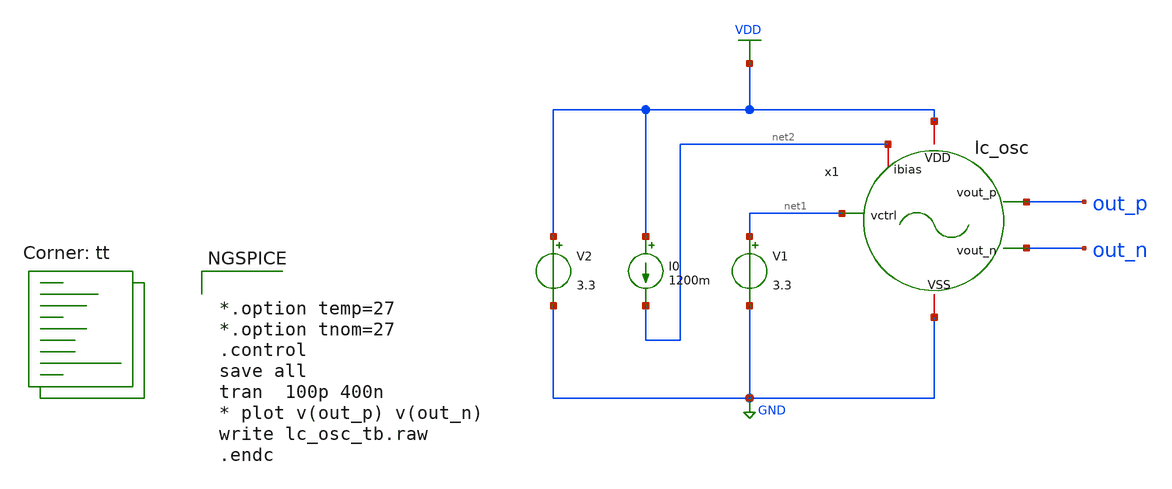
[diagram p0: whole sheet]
** sch_path: designs/libs/test_vco/lc_osc_tb.sch
* Copyright 2021 Stefan Frederik Schippers
* Licensed under the Apache License, Version 2.0 (the "License");
* you may not use this file except in compliance with the License.
* You may obtain a copy of the License at
* https://www.apache.org/licenses/LICENSE-2.0
* Unless required by applicable law or agreed to in writing, software
* distributed under the License is distributed on an "AS IS" BASIS,
* WITHOUT WARRANTIES OR CONDITIONS OF ANY KIND, either express or implied.
* See the License for the specific language governing permissions and
* limitations under the License.
**.subckt lc_osc_tb
V1 net1 GND 3.3
V2 VDD GND 3.3
I0 VDD net2 1200m
x1 VDD out_n out_p net1 GND net2 lc_osc
**** begin user architecture code


*.option temp=27
*.option tnom=27
.control
save all
tran  100p 400n
* plot v(out_p) v(out_n)
write lc_osc_tb.raw
.endc


.lib $::SKYWATER_MODELS/sky130.lib.spice tt
**** end user architecture code
**.ends

* expanding   symbol:  libs/test_vco/lc_osc.sym # of pins=6
** sym_path: designs/libs/test_vco/lc_osc.sym
** sch_path: designs/libs/test_vco/lc_osc.sch
.subckt lc_osc VDD vout_n vout_p vctrl VSS ibias
*.ipin vctrl
*.iopin VSS
*.iopin VDD
*.opin vout_p
*.opin vout_n
*.iopin ibias
L2 VDD vout_n 500p m=1
L3 VDD vout_p 500p m=1
XM4 ibias ibias VSS VSS sky130_fd_pr__nfet_g5v0d10v5 L=0.5 W=50 nf=1 ad='int((nf+1)/2) * W/nf * 0.29'
+ as='int((nf+2)/2) * W/nf * 0.29' pd='2*int((nf+1)/2) * (W/nf + 0.29)' ps='2*int((nf+2)/2) * (W/nf + 0.29)'
+ nrd='0.29 / W' nrs='0.29 / W' sa=0 sb=0 sd=0 mult=1 m=1
XM3 net1 ibias VSS VSS sky130_fd_pr__nfet_g5v0d10v5 L=0.5 W=50 nf=1 ad='int((nf+1)/2) * W/nf * 0.29'
+ as='int((nf+2)/2) * W/nf * 0.29' pd='2*int((nf+1)/2) * (W/nf + 0.29)' ps='2*int((nf+2)/2) * (W/nf + 0.29)'
+ nrd='0.29 / W' nrs='0.29 / W' sa=0 sb=0 sd=0 mult=1 m=1
XM1 vout_n vout_p net1 net1 sky130_fd_pr__nfet_g5v0d10v5 L=0.5 W=50 nf=1 ad='int((nf+1)/2) * W/nf * 0.29'
+ as='int((nf+2)/2) * W/nf * 0.29' pd='2*int((nf+1)/2) * (W/nf + 0.29)' ps='2*int((nf+2)/2) * (W/nf + 0.29)'
+ nrd='0.29 / W' nrs='0.29 / W' sa=0 sb=0 sd=0 mult=40 m=40
XM2 vout_p vout_n net1 net1 sky130_fd_pr__nfet_g5v0d10v5 L=0.5 W=50 nf=1 ad='int((nf+1)/2) * W/nf * 0.29'
+ as='int((nf+2)/2) * W/nf * 0.29' pd='2*int((nf+1)/2) * (W/nf + 0.29)' ps='2*int((nf+2)/2) * (W/nf + 0.29)'
+ nrd='0.29 / W' nrs='0.29 / W' sa=0 sb=0 sd=0 mult=40 m=40
XC1 vout_n vout_p vctrl sky130_fd_pr__cap_var_hvt W=50 L=20 VM=1 m=1
.ends

.GLOBAL VDD
.GLOBAL GND
.end
